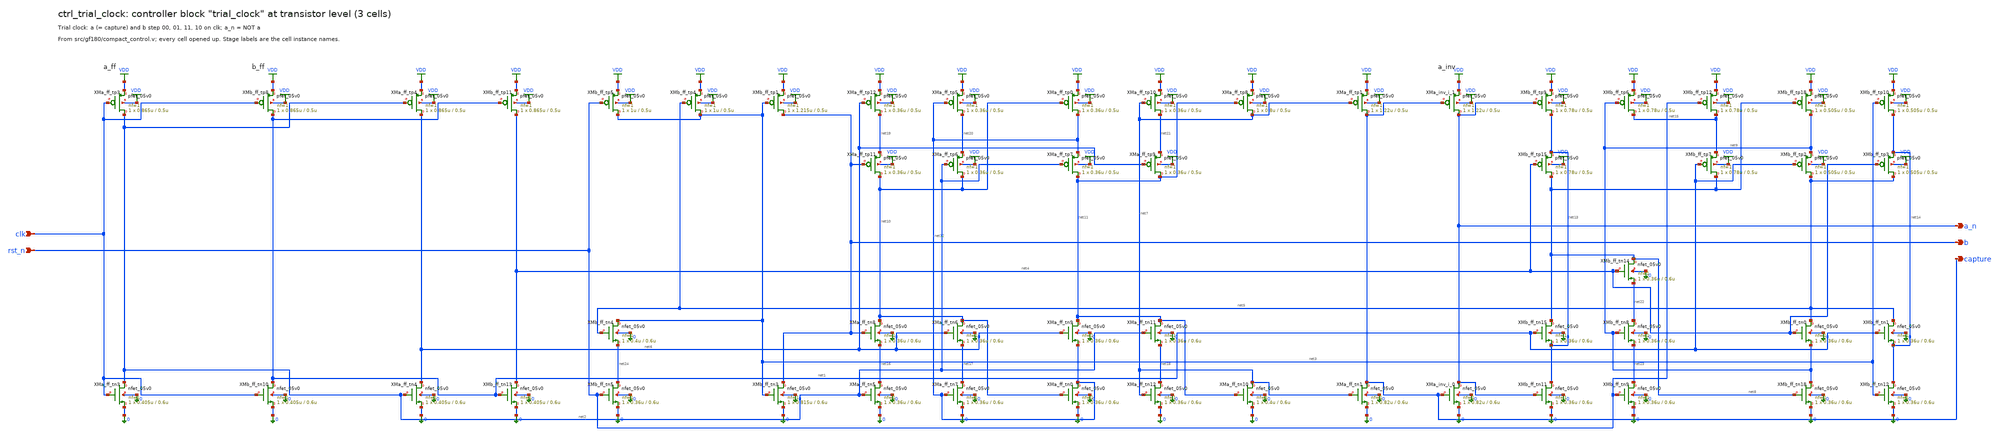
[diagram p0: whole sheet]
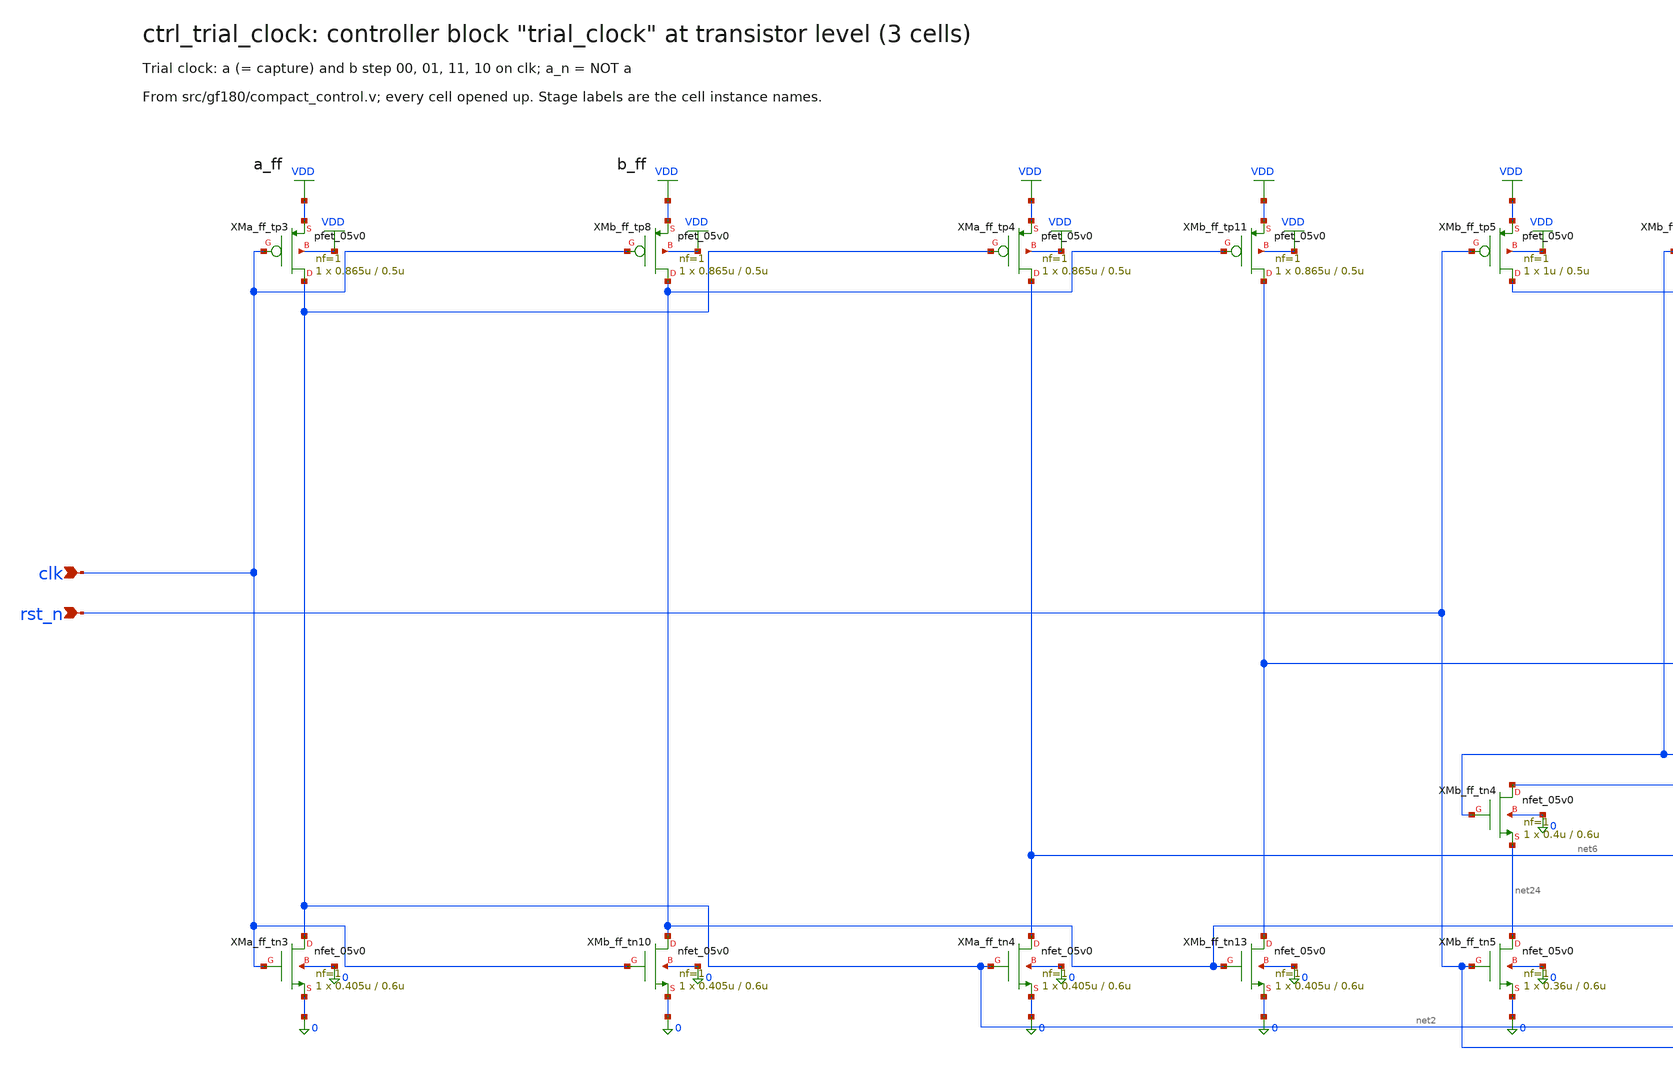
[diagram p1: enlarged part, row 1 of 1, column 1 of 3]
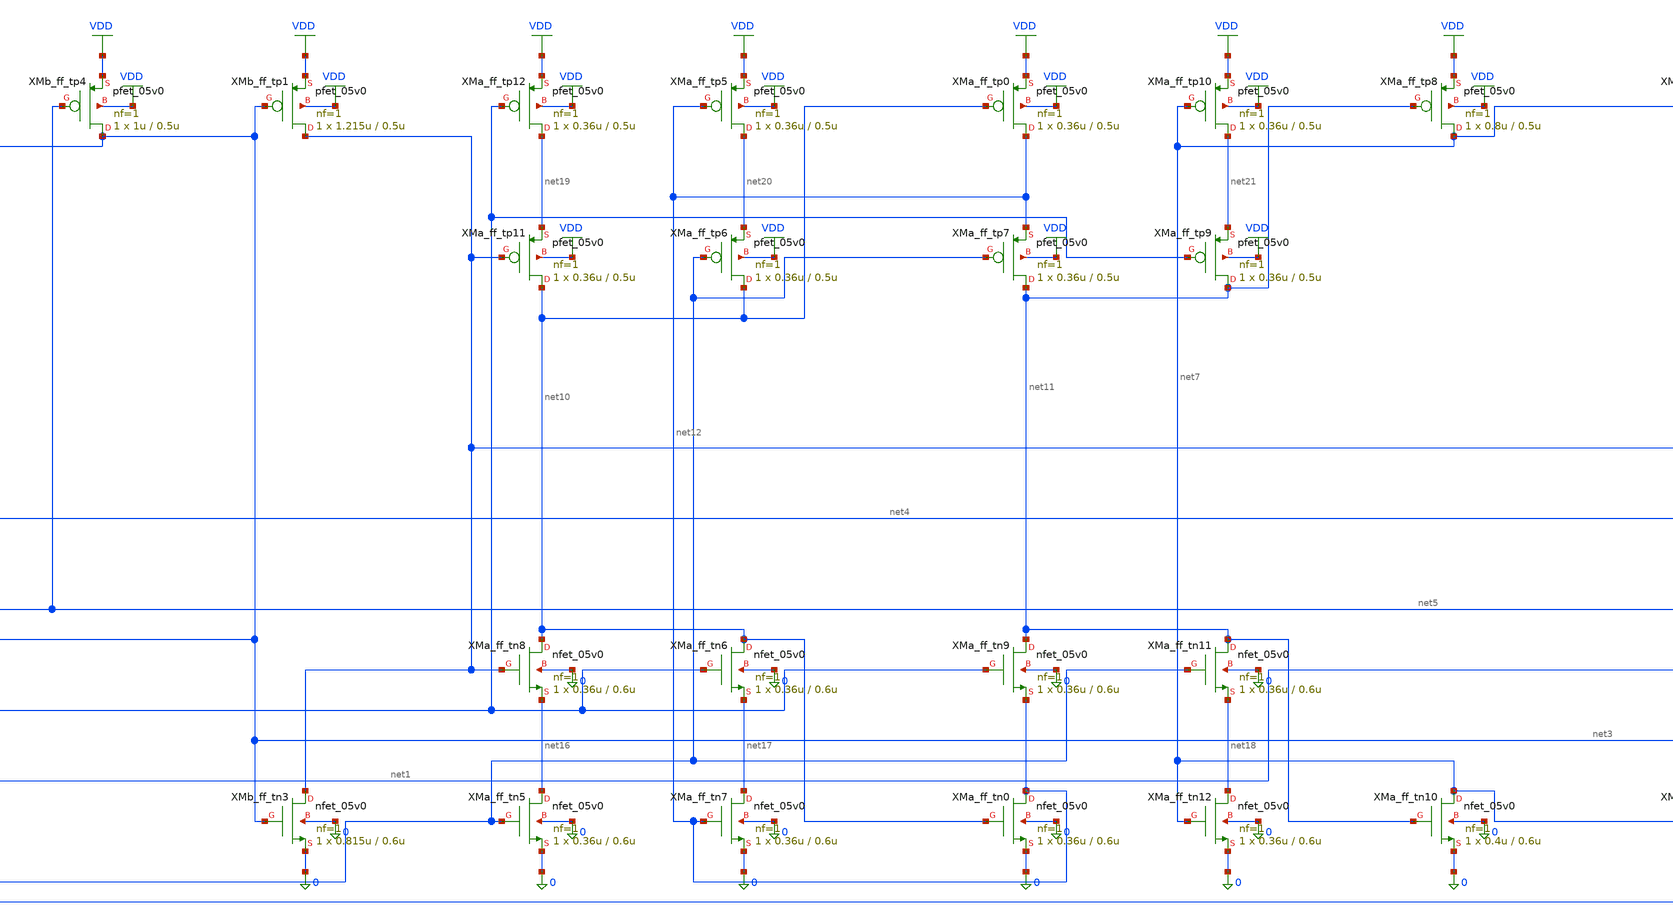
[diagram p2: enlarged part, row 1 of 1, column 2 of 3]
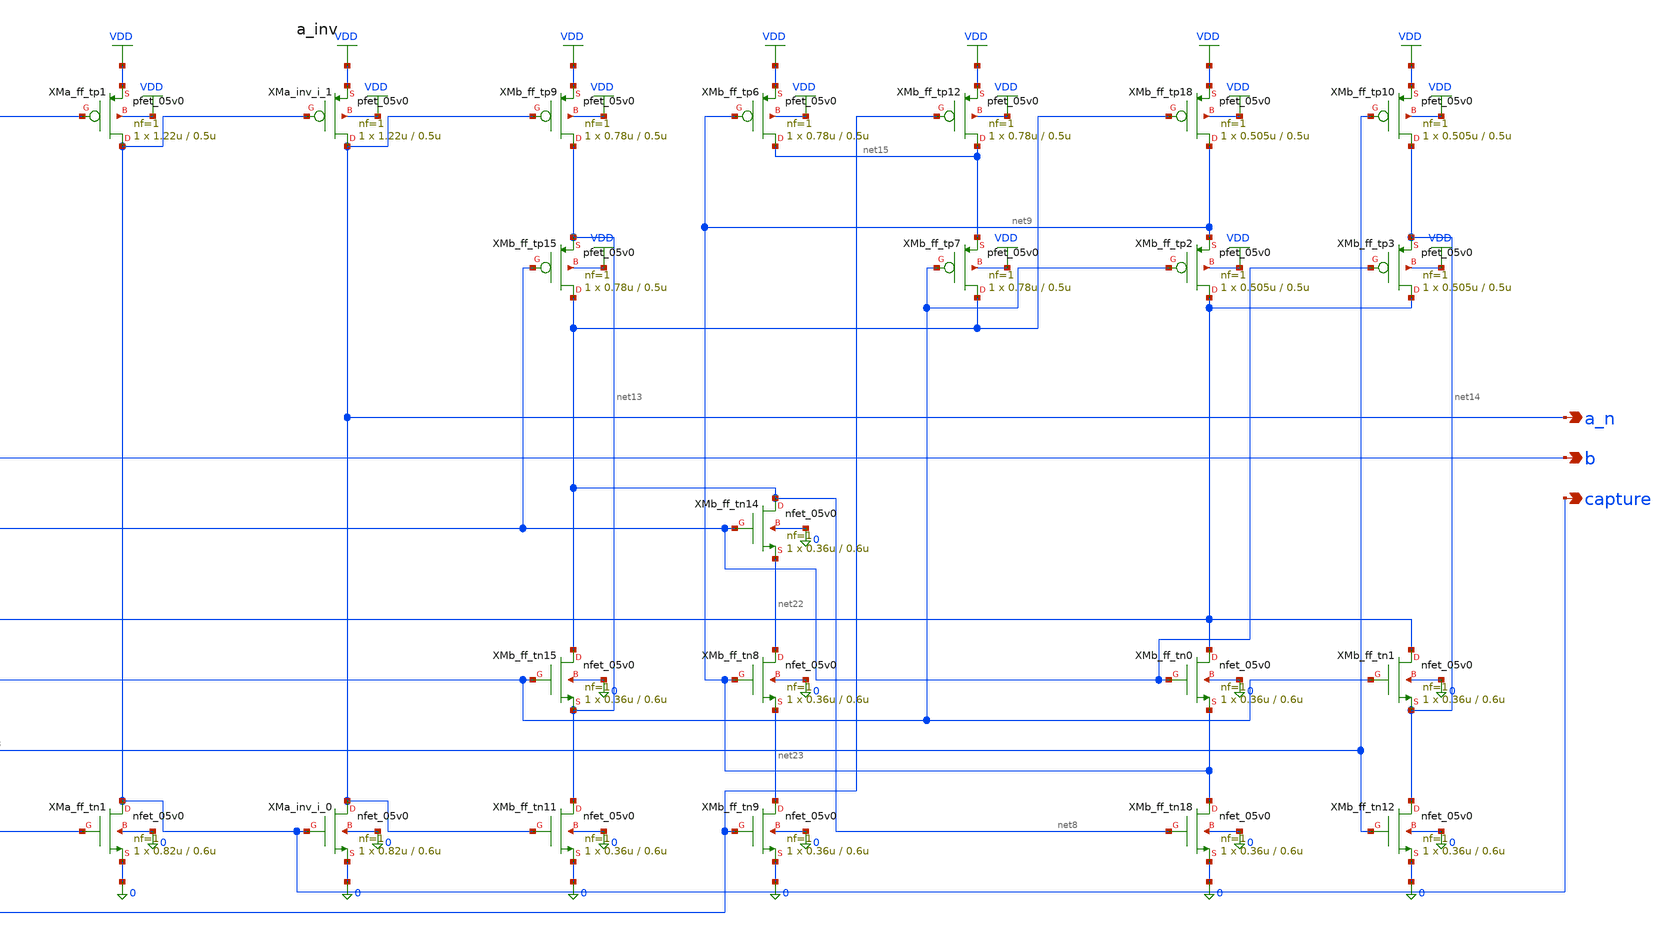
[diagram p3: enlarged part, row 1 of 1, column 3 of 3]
** sch_path: xschem/flat/ctrl_trial_clock.sch
**.subckt ctrl_trial_clock clk rst_n a_n b capture
*.ipin clk
*.ipin rst_n
*.opin a_n
*.opin b
*.opin capture
XMa_ff_tn3 net2 clk 0 0 nfet_05v0 L=0.6u W=0.405u nf=1 ad=2.025e-13 as=2.025e-13 pd=1.81e-06
+ ps=1.81e-06 nrd=0 nrs=0 sa=0 sb=0 sd=0 m=1
XMa_ff_tn4 net6 net2 0 0 nfet_05v0 L=0.6u W=0.405u nf=1 ad=2.025e-13 as=2.025e-13 pd=1.81e-06
+ ps=1.81e-06 nrd=0 nrs=0 sa=0 sb=0 sd=0 m=1
XMa_ff_tn5 net16 net2 0 0 nfet_05v0 L=0.6u W=0.36u nf=1 ad=1.8e-13 as=1.8e-13 pd=1.72e-06
+ ps=1.72e-06 nrd=0 nrs=0 sa=0 sb=0 sd=0 m=1
XMa_ff_tn8 net10 b net16 0 nfet_05v0 L=0.6u W=0.36u nf=1 ad=1.8e-13 as=1.8e-13 pd=1.72e-06
+ ps=1.72e-06 nrd=0 nrs=0 sa=0 sb=0 sd=0 m=1
XMa_ff_tn6 net10 net6 net17 0 nfet_05v0 L=0.6u W=0.36u nf=1 ad=1.8e-13 as=1.8e-13 pd=1.72e-06
+ ps=1.72e-06 nrd=0 nrs=0 sa=0 sb=0 sd=0 m=1
XMa_ff_tn7 net17 net12 0 0 nfet_05v0 L=0.6u W=0.36u nf=1 ad=1.8e-13 as=1.8e-13 pd=1.72e-06
+ ps=1.72e-06 nrd=0 nrs=0 sa=0 sb=0 sd=0 m=1
XMa_ff_tn0 net12 net10 0 0 nfet_05v0 L=0.6u W=0.36u nf=1 ad=1.8e-13 as=1.8e-13 pd=1.72e-06
+ ps=1.72e-06 nrd=0 nrs=0 sa=0 sb=0 sd=0 m=1
XMa_ff_tn9 net11 net6 net12 0 nfet_05v0 L=0.6u W=0.36u nf=1 ad=1.8e-13 as=1.8e-13 pd=1.72e-06
+ ps=1.72e-06 nrd=0 nrs=0 sa=0 sb=0 sd=0 m=1
XMa_ff_tn11 net11 net2 net18 0 nfet_05v0 L=0.6u W=0.36u nf=1 ad=1.8e-13 as=1.8e-13 pd=1.72e-06
+ ps=1.72e-06 nrd=0 nrs=0 sa=0 sb=0 sd=0 m=1
XMa_ff_tn12 net18 net7 0 0 nfet_05v0 L=0.6u W=0.36u nf=1 ad=1.8e-13 as=1.8e-13 pd=1.72e-06
+ ps=1.72e-06 nrd=0 nrs=0 sa=0 sb=0 sd=0 m=1
XMa_ff_tn10 net7 net11 0 0 nfet_05v0 L=0.6u W=0.4u nf=1 ad=2e-13 as=2e-13 pd=1.8e-06 ps=1.8e-06
+ nrd=0 nrs=0 sa=0 sb=0 sd=0 m=1
XMa_ff_tn1 capture net7 0 0 nfet_05v0 L=0.6u W=0.82u nf=1 ad=4.1e-13 as=4.1e-13 pd=2.64e-06
+ ps=2.64e-06 nrd=0 nrs=0 sa=0 sb=0 sd=0 m=1
XMa_ff_tp3 net2 clk VDD VDD pfet_05v0 L=0.5u W=0.865u nf=1 ad=4.325e-13 as=4.325e-13 pd=2.73e-06
+ ps=2.73e-06 nrd=0 nrs=0 sa=0 sb=0 sd=0 m=1
XMa_ff_tp4 net6 net2 VDD VDD pfet_05v0 L=0.5u W=0.865u nf=1 ad=4.325e-13 as=4.325e-13 pd=2.73e-06
+ ps=2.73e-06 nrd=0 nrs=0 sa=0 sb=0 sd=0 m=1
XMa_ff_tp12 net19 net6 VDD VDD pfet_05v0 L=0.5u W=0.36u nf=1 ad=1.8e-13 as=1.8e-13 pd=1.72e-06
+ ps=1.72e-06 nrd=0 nrs=0 sa=0 sb=0 sd=0 m=1
XMa_ff_tp11 net10 b net19 VDD pfet_05v0 L=0.5u W=0.36u nf=1 ad=1.8e-13 as=1.8e-13 pd=1.72e-06
+ ps=1.72e-06 nrd=0 nrs=0 sa=0 sb=0 sd=0 m=1
XMa_ff_tp6 net10 net2 net20 VDD pfet_05v0 L=0.5u W=0.36u nf=1 ad=1.8e-13 as=1.8e-13 pd=1.72e-06
+ ps=1.72e-06 nrd=0 nrs=0 sa=0 sb=0 sd=0 m=1
XMa_ff_tp5 net20 net12 VDD VDD pfet_05v0 L=0.5u W=0.36u nf=1 ad=1.8e-13 as=1.8e-13 pd=1.72e-06
+ ps=1.72e-06 nrd=0 nrs=0 sa=0 sb=0 sd=0 m=1
XMa_ff_tp0 net12 net10 VDD VDD pfet_05v0 L=0.5u W=0.36u nf=1 ad=1.8e-13 as=1.8e-13 pd=1.72e-06
+ ps=1.72e-06 nrd=0 nrs=0 sa=0 sb=0 sd=0 m=1
XMa_ff_tp7 net11 net2 net12 VDD pfet_05v0 L=0.5u W=0.36u nf=1 ad=1.8e-13 as=1.8e-13 pd=1.72e-06
+ ps=1.72e-06 nrd=0 nrs=0 sa=0 sb=0 sd=0 m=1
XMa_ff_tp9 net11 net6 net21 VDD pfet_05v0 L=0.5u W=0.36u nf=1 ad=1.8e-13 as=1.8e-13 pd=1.72e-06
+ ps=1.72e-06 nrd=0 nrs=0 sa=0 sb=0 sd=0 m=1
XMa_ff_tp10 net21 net7 VDD VDD pfet_05v0 L=0.5u W=0.36u nf=1 ad=1.8e-13 as=1.8e-13 pd=1.72e-06
+ ps=1.72e-06 nrd=0 nrs=0 sa=0 sb=0 sd=0 m=1
XMa_ff_tp8 net7 net11 VDD VDD pfet_05v0 L=0.5u W=0.8u nf=1 ad=4e-13 as=4e-13 pd=2.6e-06 ps=2.6e-06
+ nrd=0 nrs=0 sa=0 sb=0 sd=0 m=1
XMa_ff_tp1 capture net7 VDD VDD pfet_05v0 L=0.5u W=1.22u nf=1 ad=6.1e-13 as=6.1e-13 pd=3.44e-06
+ ps=3.44e-06 nrd=0 nrs=0 sa=0 sb=0 sd=0 m=1
XMa_inv_i_0 a_n capture 0 0 nfet_05v0 L=0.6u W=0.82u nf=1 ad=4.1e-13 as=4.1e-13 pd=2.64e-06
+ ps=2.64e-06 nrd=0 nrs=0 sa=0 sb=0 sd=0 m=1
XMa_inv_i_1 a_n capture VDD VDD pfet_05v0 L=0.5u W=1.22u nf=1 ad=6.1e-13 as=6.1e-13 pd=3.44e-06
+ ps=3.44e-06 nrd=0 nrs=0 sa=0 sb=0 sd=0 m=1
XMb_ff_tn10 net1 clk 0 0 nfet_05v0 L=0.6u W=0.405u nf=1 ad=2.025e-13 as=2.025e-13 pd=1.81e-06
+ ps=1.81e-06 nrd=0 nrs=0 sa=0 sb=0 sd=0 m=1
XMb_ff_tn13 net4 net1 0 0 nfet_05v0 L=0.6u W=0.405u nf=1 ad=2.025e-13 as=2.025e-13 pd=1.81e-06
+ ps=1.81e-06 nrd=0 nrs=0 sa=0 sb=0 sd=0 m=1
XMb_ff_tn11 net13 a_n 0 0 nfet_05v0 L=0.6u W=0.36u nf=1 ad=1.8e-13 as=1.8e-13 pd=1.72e-06
+ ps=1.72e-06 nrd=0 nrs=0 sa=0 sb=0 sd=0 m=1
XMb_ff_tn15 net8 net1 net13 0 nfet_05v0 L=0.6u W=0.36u nf=1 ad=1.8e-13 as=1.8e-13 pd=1.72e-06
+ ps=1.72e-06 nrd=0 nrs=0 sa=0 sb=0 sd=0 m=1
XMb_ff_tn14 net8 net4 net22 0 nfet_05v0 L=0.6u W=0.36u nf=1 ad=1.8e-13 as=1.8e-13 pd=1.72e-06
+ ps=1.72e-06 nrd=0 nrs=0 sa=0 sb=0 sd=0 m=1
XMb_ff_tn8 net22 net9 net23 0 nfet_05v0 L=0.6u W=0.36u nf=1 ad=1.8e-13 as=1.8e-13 pd=1.72e-06
+ ps=1.72e-06 nrd=0 nrs=0 sa=0 sb=0 sd=0 m=1
XMb_ff_tn9 net23 rst_n 0 0 nfet_05v0 L=0.6u W=0.36u nf=1 ad=1.8e-13 as=1.8e-13 pd=1.72e-06
+ ps=1.72e-06 nrd=0 nrs=0 sa=0 sb=0 sd=0 m=1
XMb_ff_tn18 net9 net8 0 0 nfet_05v0 L=0.6u W=0.36u nf=1 ad=1.8e-13 as=1.8e-13 pd=1.72e-06
+ ps=1.72e-06 nrd=0 nrs=0 sa=0 sb=0 sd=0 m=1
XMb_ff_tn0 net5 net4 net9 0 nfet_05v0 L=0.6u W=0.36u nf=1 ad=1.8e-13 as=1.8e-13 pd=1.72e-06
+ ps=1.72e-06 nrd=0 nrs=0 sa=0 sb=0 sd=0 m=1
XMb_ff_tn1 net5 net1 net14 0 nfet_05v0 L=0.6u W=0.36u nf=1 ad=1.8e-13 as=1.8e-13 pd=1.72e-06
+ ps=1.72e-06 nrd=0 nrs=0 sa=0 sb=0 sd=0 m=1
XMb_ff_tn12 net14 net3 0 0 nfet_05v0 L=0.6u W=0.36u nf=1 ad=1.8e-13 as=1.8e-13 pd=1.72e-06
+ ps=1.72e-06 nrd=0 nrs=0 sa=0 sb=0 sd=0 m=1
XMb_ff_tn5 net24 rst_n 0 0 nfet_05v0 L=0.6u W=0.36u nf=1 ad=1.8e-13 as=1.8e-13 pd=1.72e-06
+ ps=1.72e-06 nrd=0 nrs=0 sa=0 sb=0 sd=0 m=1
XMb_ff_tn4 net3 net5 net24 0 nfet_05v0 L=0.6u W=0.4u nf=1 ad=2e-13 as=2e-13 pd=1.8e-06 ps=1.8e-06
+ nrd=0 nrs=0 sa=0 sb=0 sd=0 m=1
XMb_ff_tn3 b net3 0 0 nfet_05v0 L=0.6u W=0.815u nf=1 ad=4.075e-13 as=4.075e-13 pd=2.63e-06
+ ps=2.63e-06 nrd=0 nrs=0 sa=0 sb=0 sd=0 m=1
XMb_ff_tp8 net1 clk VDD VDD pfet_05v0 L=0.5u W=0.865u nf=1 ad=4.325e-13 as=4.325e-13 pd=2.73e-06
+ ps=2.73e-06 nrd=0 nrs=0 sa=0 sb=0 sd=0 m=1
XMb_ff_tp11 net4 net1 VDD VDD pfet_05v0 L=0.5u W=0.865u nf=1 ad=4.325e-13 as=4.325e-13 pd=2.73e-06
+ ps=2.73e-06 nrd=0 nrs=0 sa=0 sb=0 sd=0 m=1
XMb_ff_tp9 net13 a_n VDD VDD pfet_05v0 L=0.5u W=0.78u nf=1 ad=3.9e-13 as=3.9e-13 pd=2.56e-06
+ ps=2.56e-06 nrd=0 nrs=0 sa=0 sb=0 sd=0 m=1
XMb_ff_tp15 net8 net4 net13 VDD pfet_05v0 L=0.5u W=0.78u nf=1 ad=3.9e-13 as=3.9e-13 pd=2.56e-06
+ ps=2.56e-06 nrd=0 nrs=0 sa=0 sb=0 sd=0 m=1
XMb_ff_tp7 net8 net1 net15 VDD pfet_05v0 L=0.5u W=0.78u nf=1 ad=3.9e-13 as=3.9e-13 pd=2.56e-06
+ ps=2.56e-06 nrd=0 nrs=0 sa=0 sb=0 sd=0 m=1
XMb_ff_tp6 net15 net9 VDD VDD pfet_05v0 L=0.5u W=0.78u nf=1 ad=3.9e-13 as=3.9e-13 pd=2.56e-06
+ ps=2.56e-06 nrd=0 nrs=0 sa=0 sb=0 sd=0 m=1
XMb_ff_tp12 net15 rst_n VDD VDD pfet_05v0 L=0.5u W=0.78u nf=1 ad=3.9e-13 as=3.9e-13 pd=2.56e-06
+ ps=2.56e-06 nrd=0 nrs=0 sa=0 sb=0 sd=0 m=1
XMb_ff_tp18 net9 net8 VDD VDD pfet_05v0 L=0.5u W=0.505u nf=1 ad=2.525e-13 as=2.525e-13 pd=2.01e-06
+ ps=2.01e-06 nrd=0 nrs=0 sa=0 sb=0 sd=0 m=1
XMb_ff_tp2 net5 net1 net9 VDD pfet_05v0 L=0.5u W=0.505u nf=1 ad=2.525e-13 as=2.525e-13 pd=2.01e-06
+ ps=2.01e-06 nrd=0 nrs=0 sa=0 sb=0 sd=0 m=1
XMb_ff_tp3 net5 net4 net14 VDD pfet_05v0 L=0.5u W=0.505u nf=1 ad=2.525e-13 as=2.525e-13 pd=2.01e-06
+ ps=2.01e-06 nrd=0 nrs=0 sa=0 sb=0 sd=0 m=1
XMb_ff_tp10 net14 net3 VDD VDD pfet_05v0 L=0.5u W=0.505u nf=1 ad=2.525e-13 as=2.525e-13 pd=2.01e-06
+ ps=2.01e-06 nrd=0 nrs=0 sa=0 sb=0 sd=0 m=1
XMb_ff_tp5 net3 rst_n VDD VDD pfet_05v0 L=0.5u W=1u nf=1 ad=5e-13 as=5e-13 pd=3e-06 ps=3e-06 nrd=0
+ nrs=0 sa=0 sb=0 sd=0 m=1
XMb_ff_tp4 net3 net5 VDD VDD pfet_05v0 L=0.5u W=1u nf=1 ad=5e-13 as=5e-13 pd=3e-06 ps=3e-06 nrd=0
+ nrs=0 sa=0 sb=0 sd=0 m=1
XMb_ff_tp1 b net3 VDD VDD pfet_05v0 L=0.5u W=1.215u nf=1 ad=6.075e-13 as=6.075e-13 pd=3.43e-06
+ ps=3.43e-06 nrd=0 nrs=0 sa=0 sb=0 sd=0 m=1
**.ends
.GLOBAL VDD
.end
